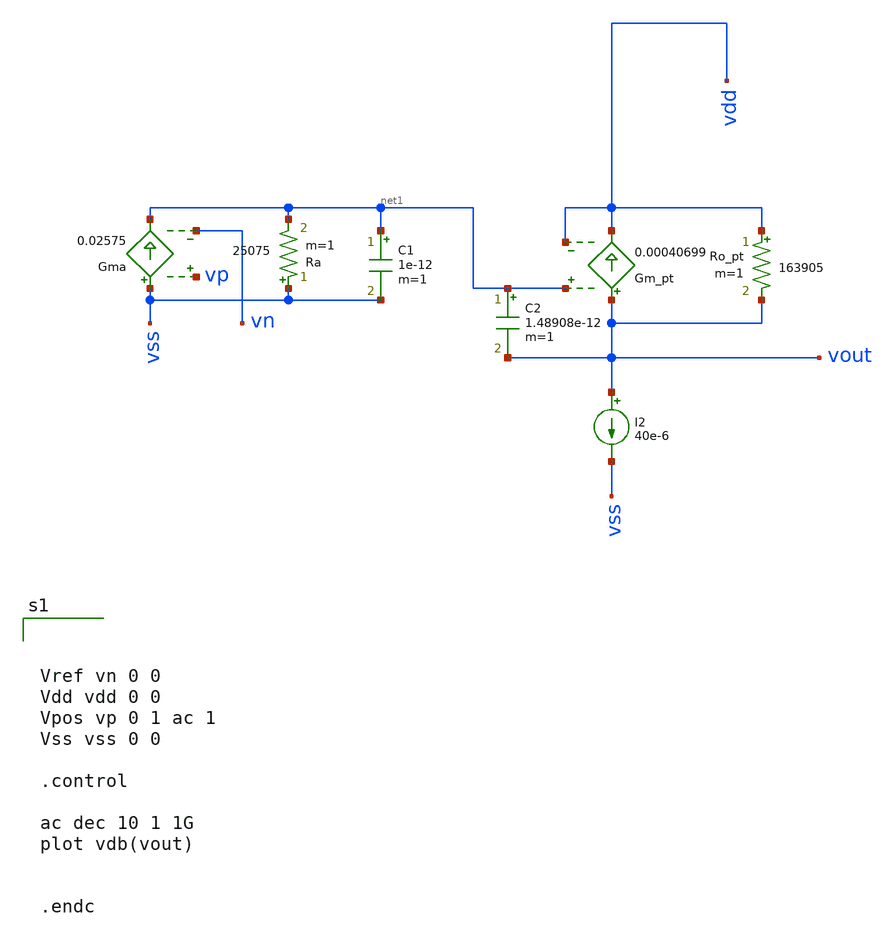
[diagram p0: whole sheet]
** sch_path: test/sstadex/xschem/stage2_OTA_tb.sch
**.subckt stage2_OTA_tb
Ro_pt vdd vout 163905 m=1
Gm_pt vout vdd net1 vdd 0.00040699
Gma vss net1 vp vn 0.02575
Ra vss net1 25075 m=1
I2 vout vss 40e-6
C1 net1 vss 1e-12 m=1
C2 net1 vout 1.48908e-12 m=1
**** begin user architecture code



Vref vn 0 0
Vdd vdd 0 0
Vpos vp 0 1 ac 1
Vss vss 0 0

.control

ac dec 10 1 1G
plot vdb(vout)


.endc



**** end user architecture code
**.ends
.end
